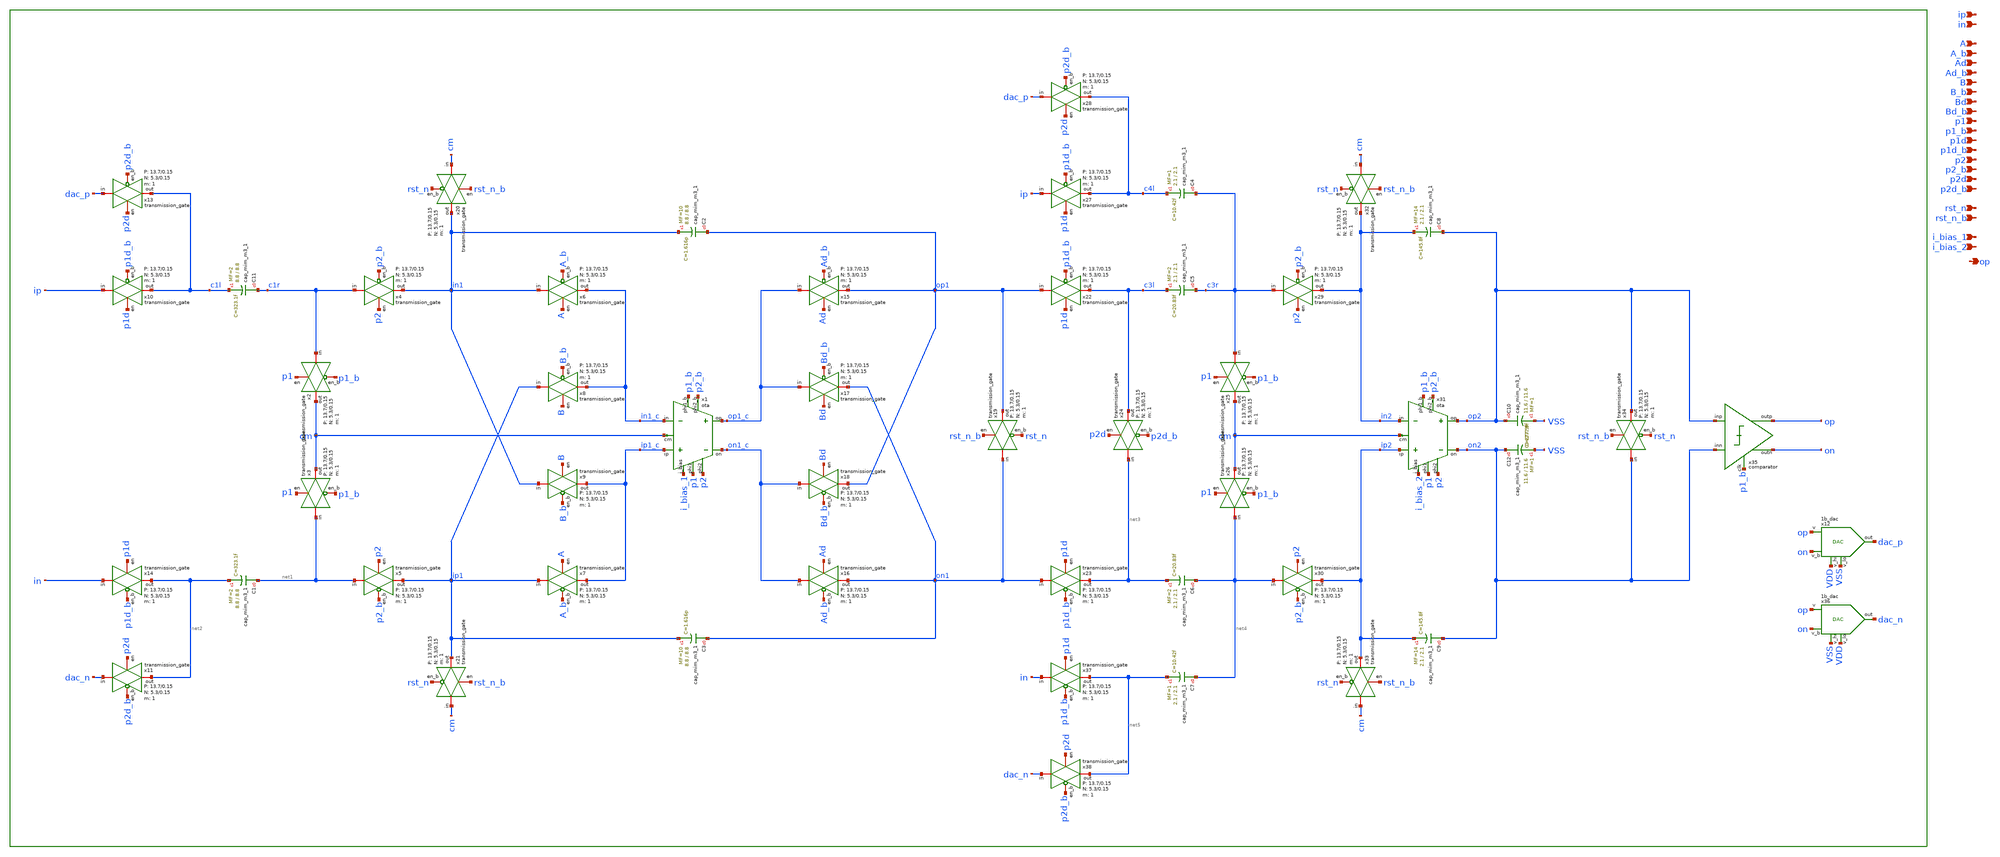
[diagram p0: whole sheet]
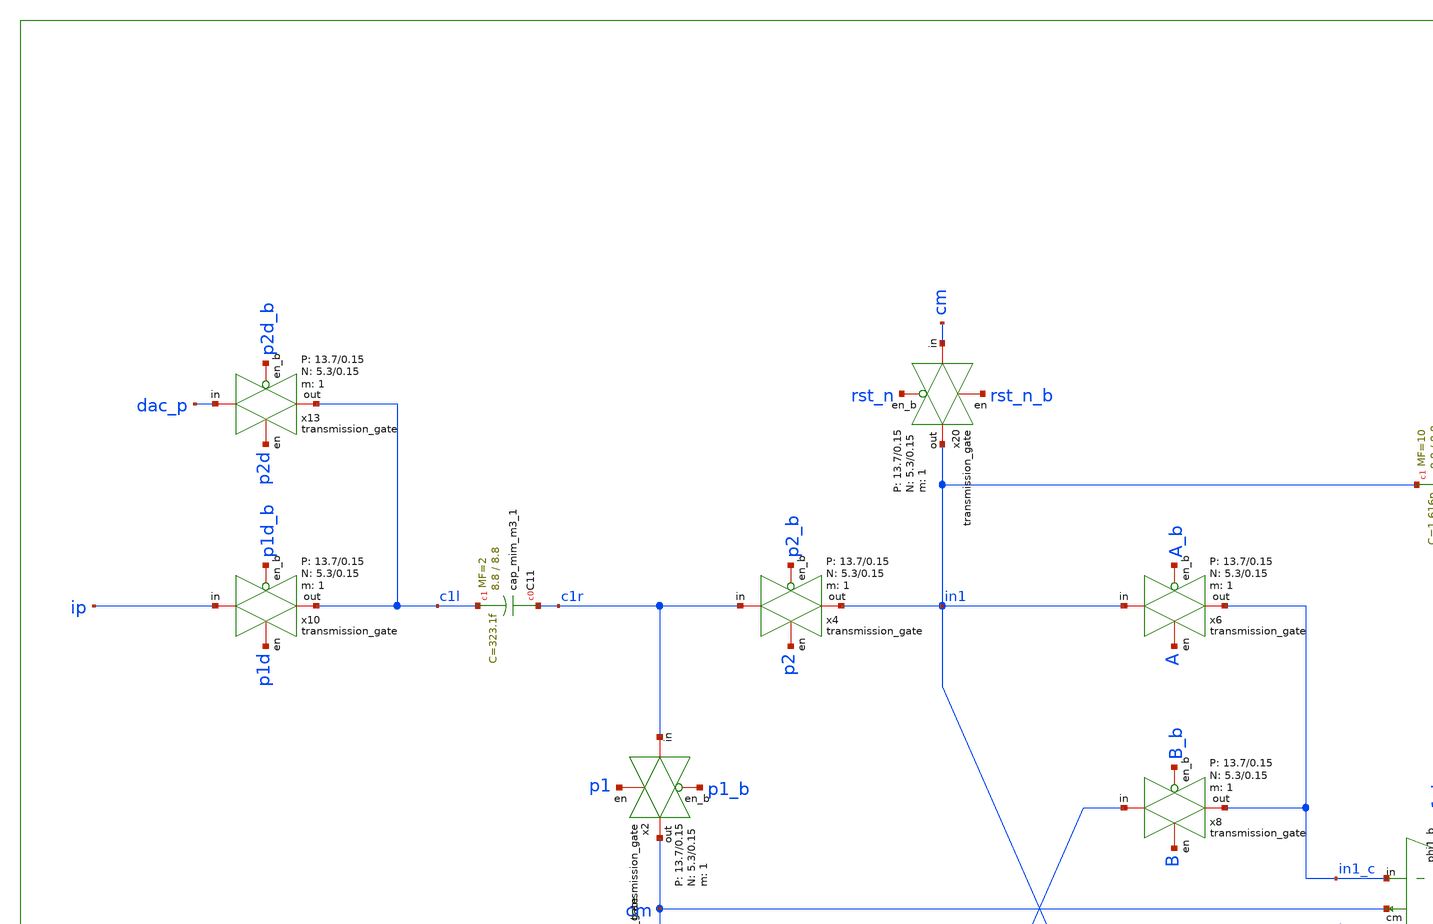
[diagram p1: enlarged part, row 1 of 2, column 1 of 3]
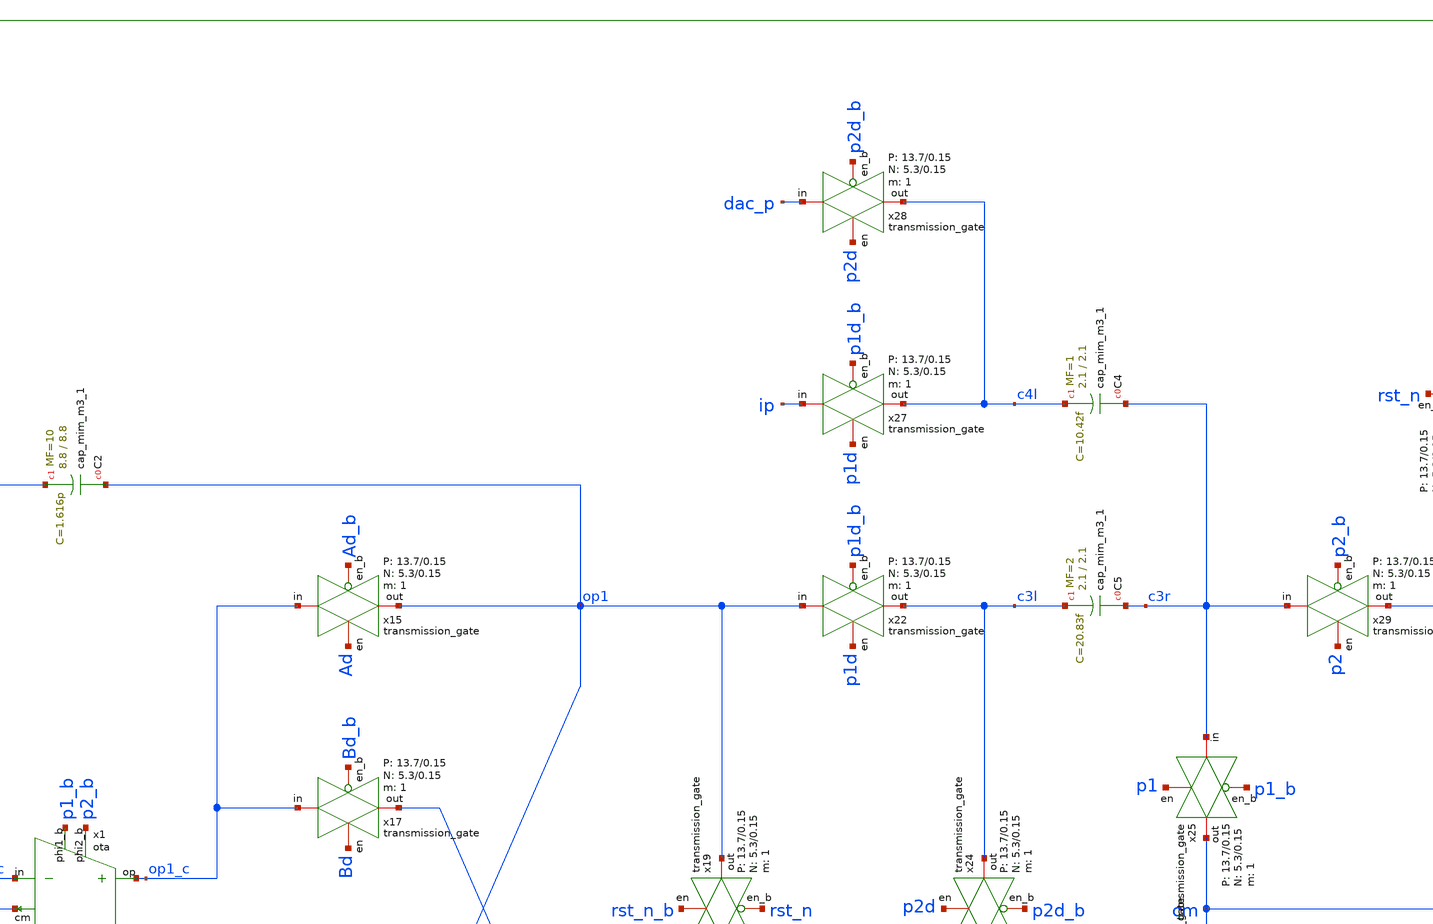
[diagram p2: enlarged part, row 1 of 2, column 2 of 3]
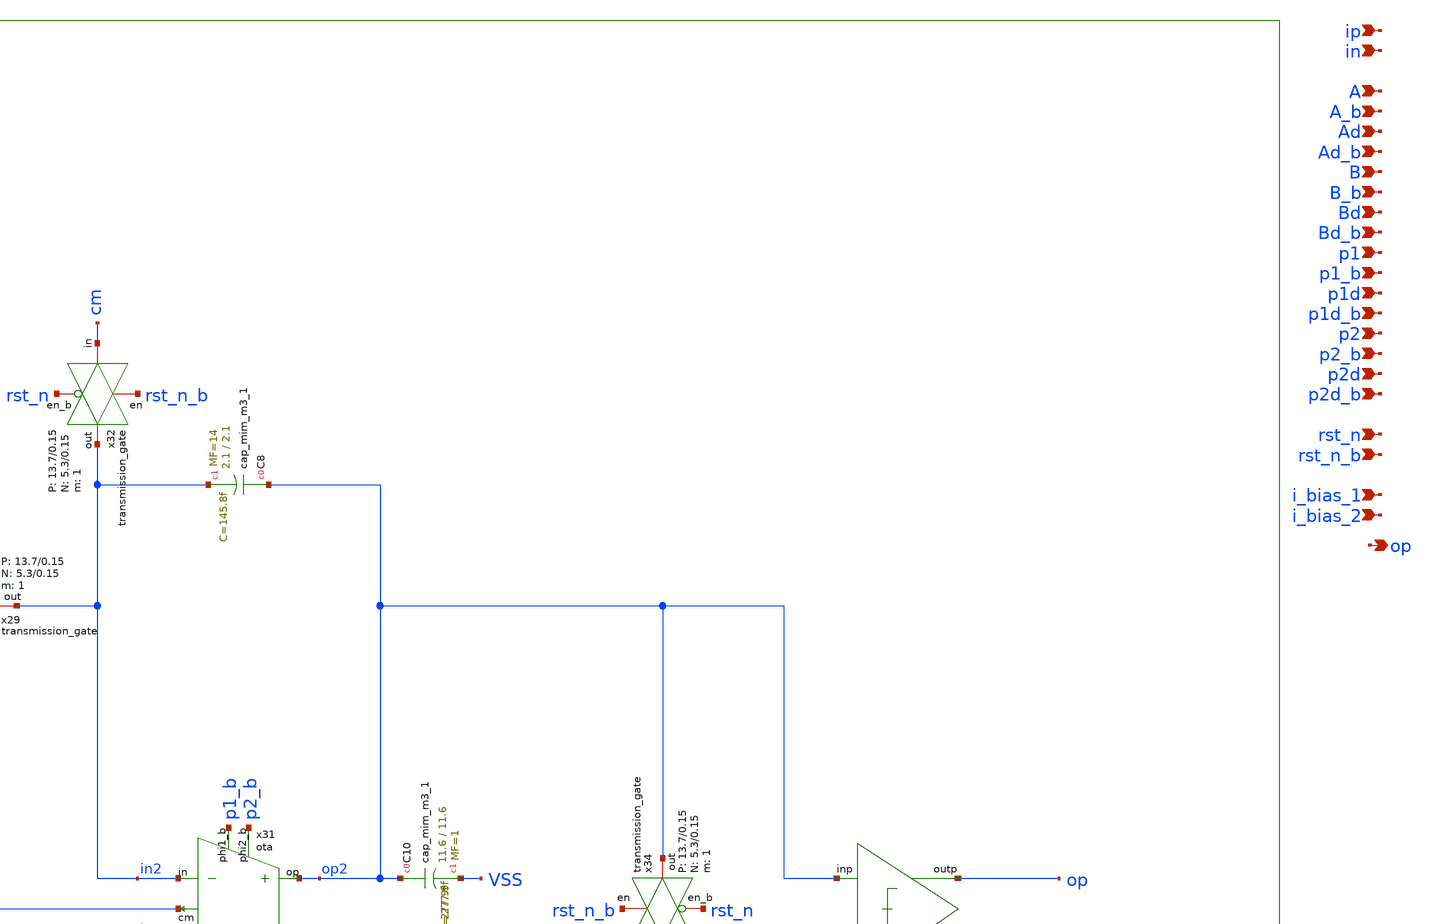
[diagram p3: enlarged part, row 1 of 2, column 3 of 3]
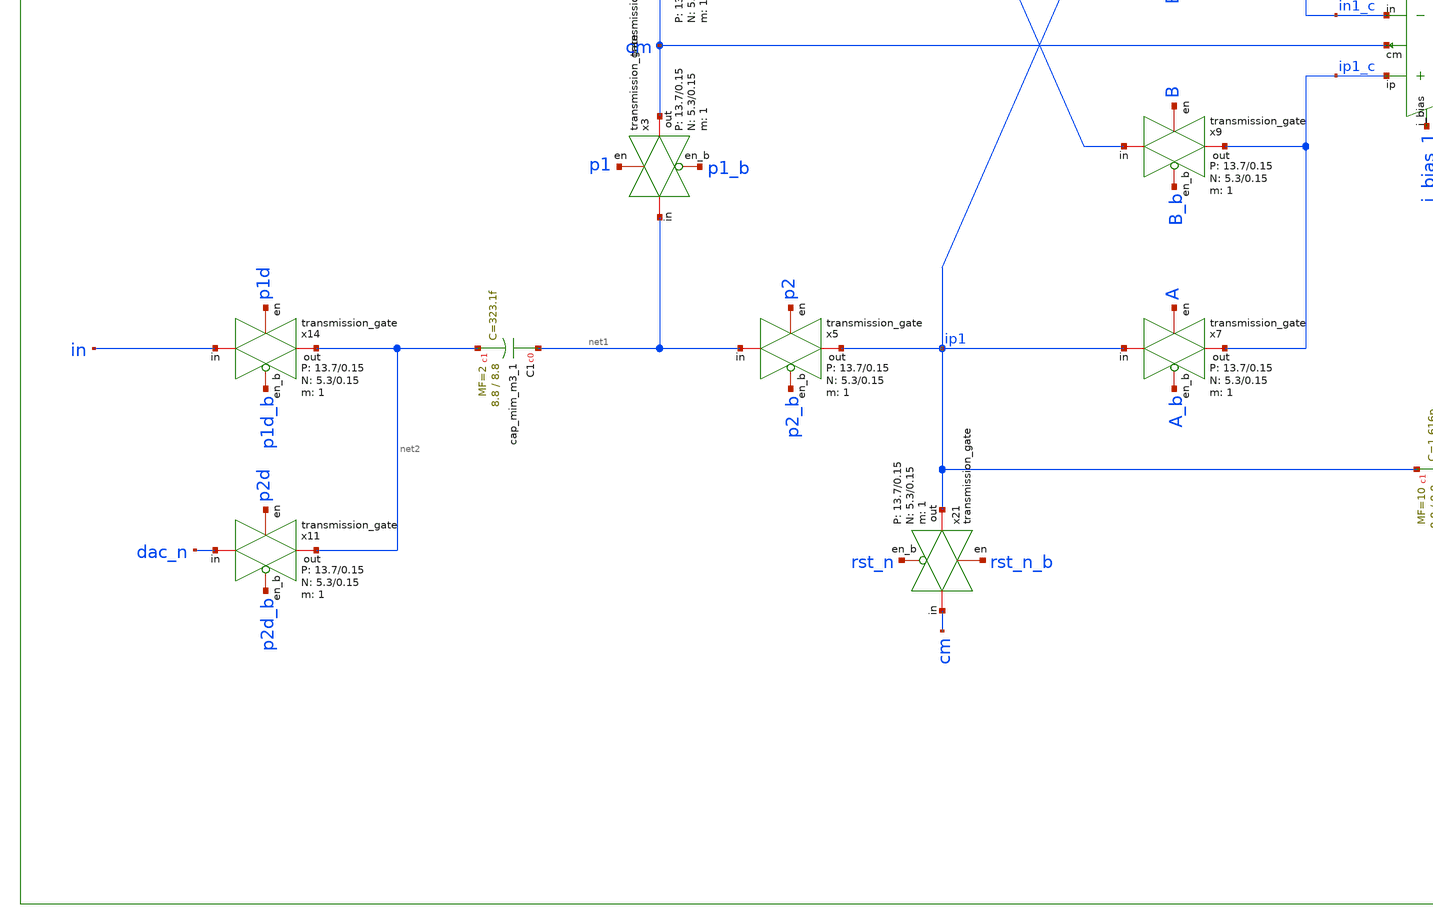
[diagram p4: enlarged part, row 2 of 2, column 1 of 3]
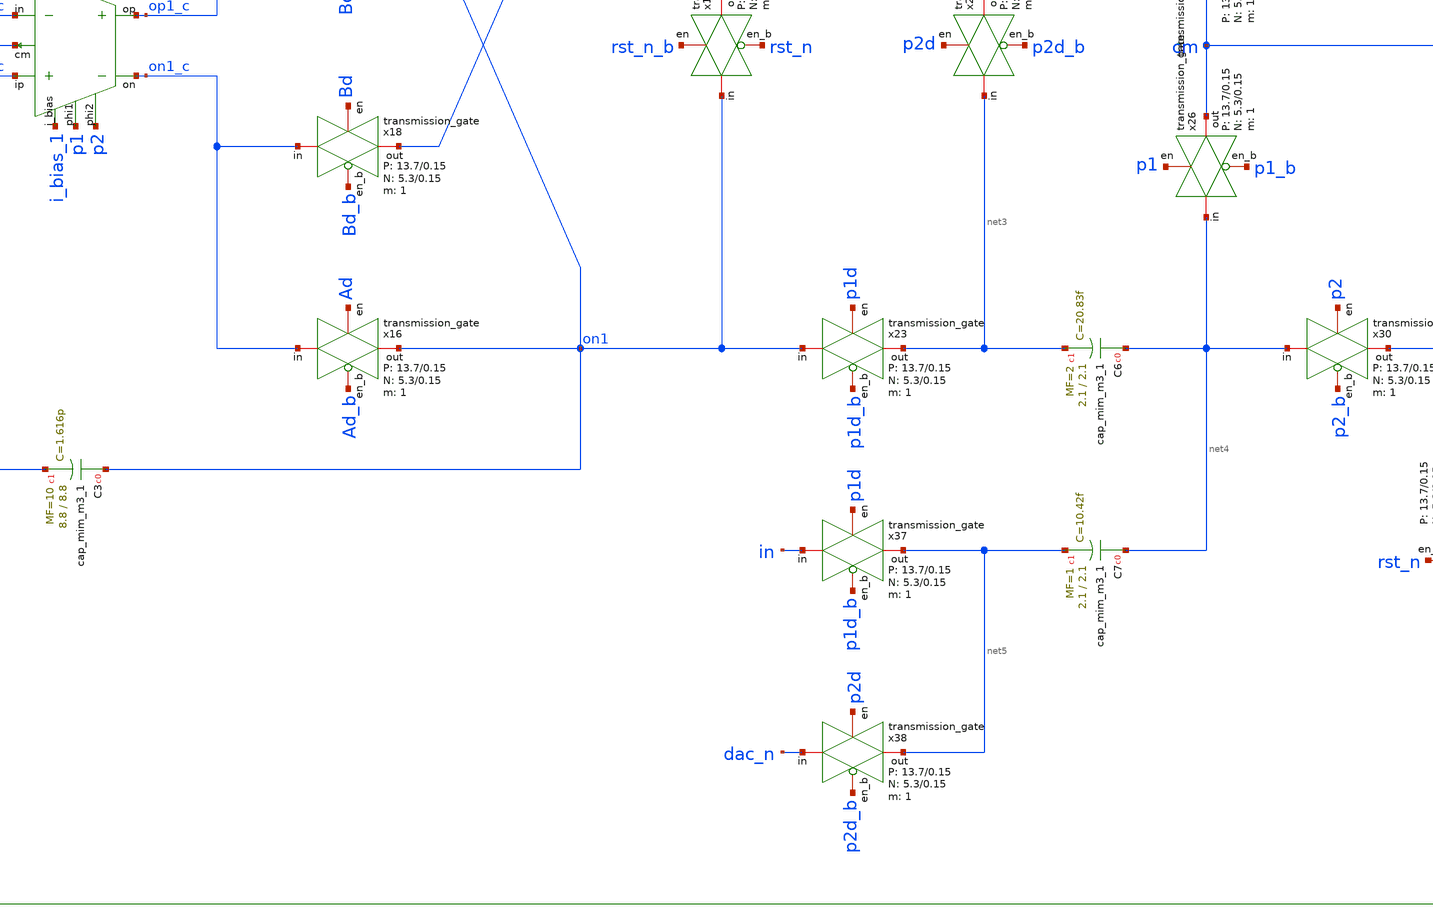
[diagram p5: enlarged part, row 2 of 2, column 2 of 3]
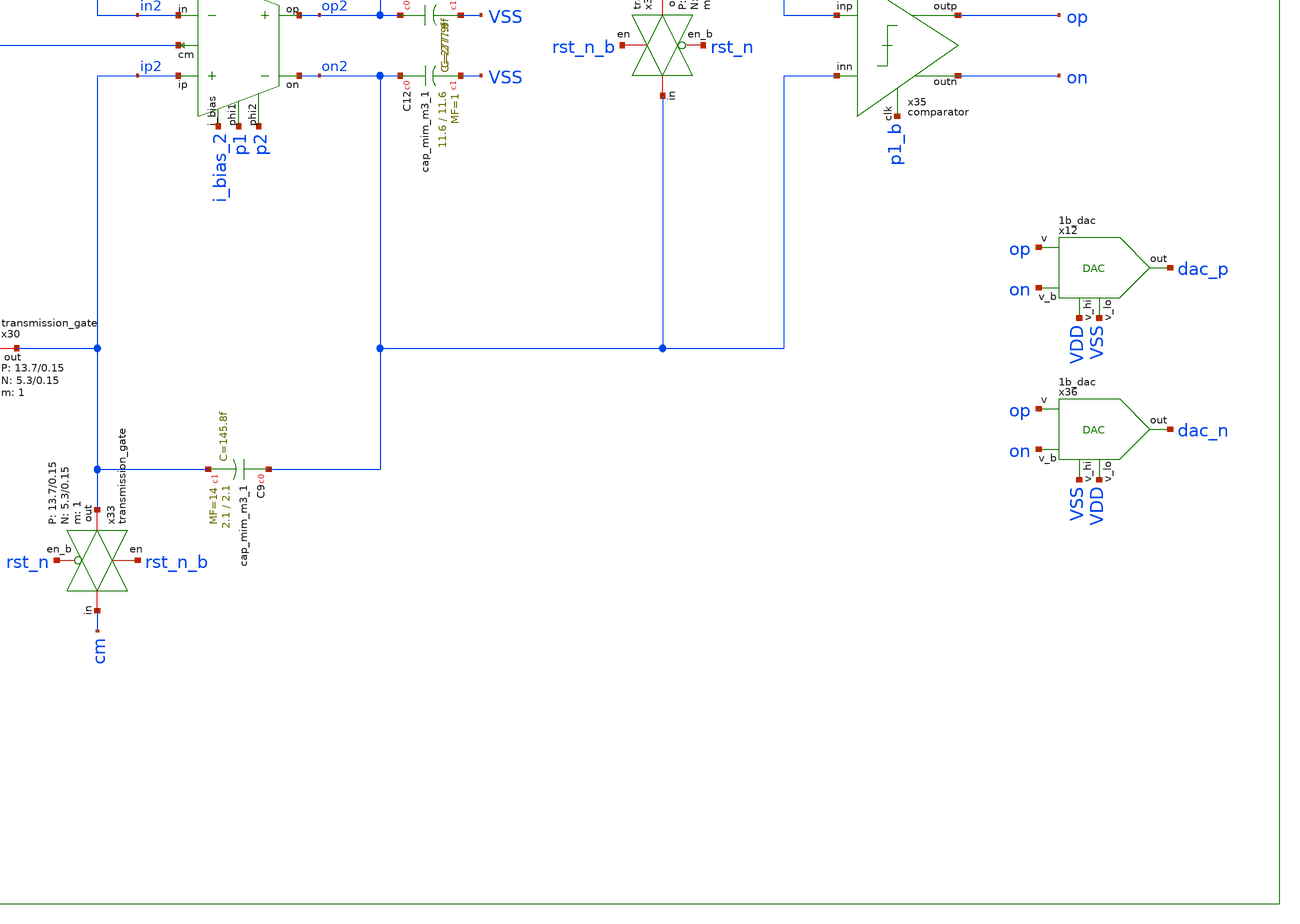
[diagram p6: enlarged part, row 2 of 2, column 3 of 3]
** sch_path: design/analog_modulator/schematic/modulator.sch
**.subckt modulator ip in A A_b Ad Ad_b B B_b Bd Bd_b p1 p1_b p1d p1d_b p2 p2_b p2d p2d_b rst_n
*+ rst_n_b i_bias_1 i_bias_2 op
*.ipin ip
*.ipin in
*.ipin A
*.ipin A_b
*.ipin Ad
*.ipin Ad_b
*.ipin B
*.ipin B_b
*.ipin Bd
*.ipin Bd_b
*.ipin p1
*.ipin p1_b
*.ipin p1d
*.ipin p1d_b
*.ipin p2
*.ipin p2_b
*.ipin p2d
*.ipin p2d_b
*.ipin rst_n
*.ipin rst_n_b
*.ipin i_bias_1
*.ipin i_bias_2
*.opin op
x4 c1r in1 p2 p2_b VDD VSS 1 5.3 0.15 13.7 0.15 transmission_gate
x5 net1 ip1 p2 p2_b VDD VSS 1 5.3 0.15 13.7 0.15 transmission_gate
x2 c1r cm p1 p1_b VDD VSS 1 5.3 0.15 13.7 0.15 transmission_gate
x3 net1 cm p1 p1_b VDD VSS 1 5.3 0.15 13.7 0.15 transmission_gate
x10 ip c1l p1d p1d_b VDD VSS 1 5.3 0.15 13.7 0.15 transmission_gate
x11 dac_n net2 p2d p2d_b VDD VSS 1 5.3 0.15 13.7 0.15 transmission_gate
x12 VDD VSS op dac_p on VDD VSS 1b_dac
x13 dac_p c1l p2d p2d_b VDD VSS 1 5.3 0.15 13.7 0.15 transmission_gate
x14 in net2 p1d p1d_b VDD VSS 1 5.3 0.15 13.7 0.15 transmission_gate
x19 on1 op1 rst_n_b rst_n VDD VSS 1 5.3 0.15 13.7 0.15 transmission_gate
x20 cm in1 rst_n_b rst_n VDD VSS 1 5.3 0.15 13.7 0.15 transmission_gate
x21 cm ip1 rst_n_b rst_n VDD VSS 1 5.3 0.15 13.7 0.15 transmission_gate
x22 op1 c3l p1d p1d_b VDD VSS 1 5.3 0.15 13.7 0.15 transmission_gate
x23 on1 net3 p1d p1d_b VDD VSS 1 5.3 0.15 13.7 0.15 transmission_gate
x24 net3 c3l p2d p2d_b VDD VSS 1 5.3 0.15 13.7 0.15 transmission_gate
x25 c3r cm p1 p1_b VDD VSS 1 5.3 0.15 13.7 0.15 transmission_gate
x26 net4 cm p1 p1_b VDD VSS 1 5.3 0.15 13.7 0.15 transmission_gate
x27 ip c4l p1d p1d_b VDD VSS 1 5.3 0.15 13.7 0.15 transmission_gate
x28 dac_p c4l p2d p2d_b VDD VSS 1 5.3 0.15 13.7 0.15 transmission_gate
x29 c3r in2 p2 p2_b VDD VSS 1 5.3 0.15 13.7 0.15 transmission_gate
x30 net4 ip2 p2 p2_b VDD VSS 1 5.3 0.15 13.7 0.15 transmission_gate
x32 cm in2 rst_n_b rst_n VDD VSS 1 5.3 0.15 13.7 0.15 transmission_gate
x33 cm ip2 rst_n_b rst_n VDD VSS 1 5.3 0.15 13.7 0.15 transmission_gate
x34 on2 op2 rst_n_b rst_n VDD VSS 1 5.3 0.15 13.7 0.15 transmission_gate
x36 VSS VDD op dac_n on VDD VSS 1b_dac
x37 in net5 p1d p1d_b VDD VSS 1 5.3 0.15 13.7 0.15 transmission_gate
x38 dac_n net5 p2d p2d_b VDD VSS 1 5.3 0.15 13.7 0.15 transmission_gate
XC11 c1r c1l sky130_fd_pr__cap_mim_m3_1 W=8.8 L=8.8 MF=2 m=2
XC1 net1 net2 sky130_fd_pr__cap_mim_m3_1 W=8.8 L=8.8 MF=2 m=2
XC2 op1 in1 sky130_fd_pr__cap_mim_m3_1 W=8.8 L=8.8 MF=10 m=10
XC3 on1 ip1 sky130_fd_pr__cap_mim_m3_1 W=8.8 L=8.8 MF=10 m=10
XC4 c3r c4l sky130_fd_pr__cap_mim_m3_1 W=2.1 L=2.1 MF=1 m=1
XC5 c3r c3l sky130_fd_pr__cap_mim_m3_1 W=2.1 L=2.1 MF=2 m=2
XC6 net4 net3 sky130_fd_pr__cap_mim_m3_1 W=2.1 L=2.1 MF=2 m=2
XC7 net4 net5 sky130_fd_pr__cap_mim_m3_1 W=2.1 L=2.1 MF=1 m=1
XC8 op2 in2 sky130_fd_pr__cap_mim_m3_1 W=2.1 L=2.1 MF=14 m=14
XC9 on2 ip2 sky130_fd_pr__cap_mim_m3_1 W=2.1 L=2.1 MF=14 m=14
XC10 op2 VSS sky130_fd_pr__cap_mim_m3_1 W=11.6 L=11.6 MF=1 m=1
XC12 on2 VSS sky130_fd_pr__cap_mim_m3_1 W=11.6 L=11.6 MF=1 m=1
x6 in1 in1_c A A_b VDD VSS 1 5.3 0.15 13.7 0.15 transmission_gate
x8 ip1 in1_c B B_b VDD VSS 1 5.3 0.15 13.7 0.15 transmission_gate
x15 op1_c op1 Ad Ad_b VDD VSS 1 5.3 0.15 13.7 0.15 transmission_gate
x16 on1_c on1 Ad Ad_b VDD VSS 1 5.3 0.15 13.7 0.15 transmission_gate
x17 op1_c on1 Bd Bd_b VDD VSS 1 5.3 0.15 13.7 0.15 transmission_gate
x18 on1_c op1 Bd Bd_b VDD VSS 1 5.3 0.15 13.7 0.15 transmission_gate
x1 i_bias_1 ip1_c in1_c p1 p1_b p2 p2_b op1_c on1_c cm VDD VSS ota
x31 i_bias_2 ip2 in2 p1 p1_b p2 p2_b op2 on2 cm VDD VSS ota
x35 op2 on2 op p1_b on VDD VSS comparator
x7 ip1 ip1_c A A_b VDD VSS 1 5.3 0.15 13.7 0.15 transmission_gate
x9 in1 ip1_c B B_b VDD VSS 1 5.3 0.15 13.7 0.15 transmission_gate
**.ends
.end
